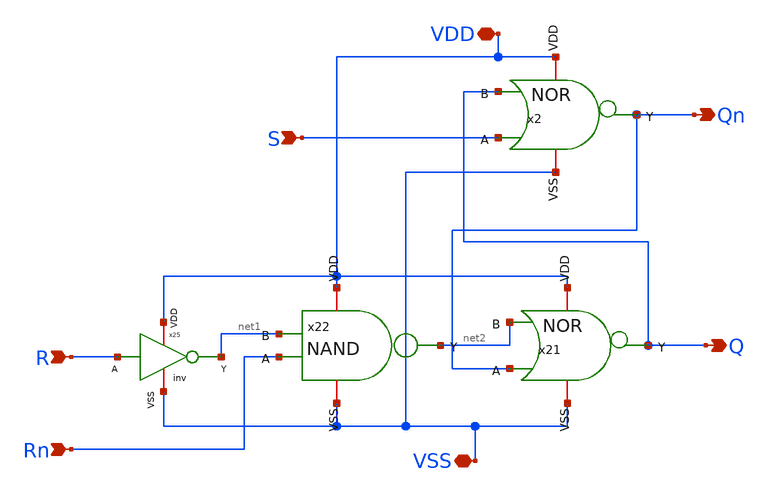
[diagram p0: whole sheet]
** sch_path: netlist/LatchJK.sch
**.subckt LatchJK Qn Rn VDD VSS R S Q
*.opin Qn
*.ipin Rn
*.iopin VDD
*.iopin VSS
*.ipin R
*.ipin S
*.opin Q
x2 VDD Q S Qn VSS NOR
x21 VDD net2 Qn Q VSS NOR
x22 VDD net1 Rn net2 VSS NAND
x25 VDD net1 R VSS inv
**.ends
.end
